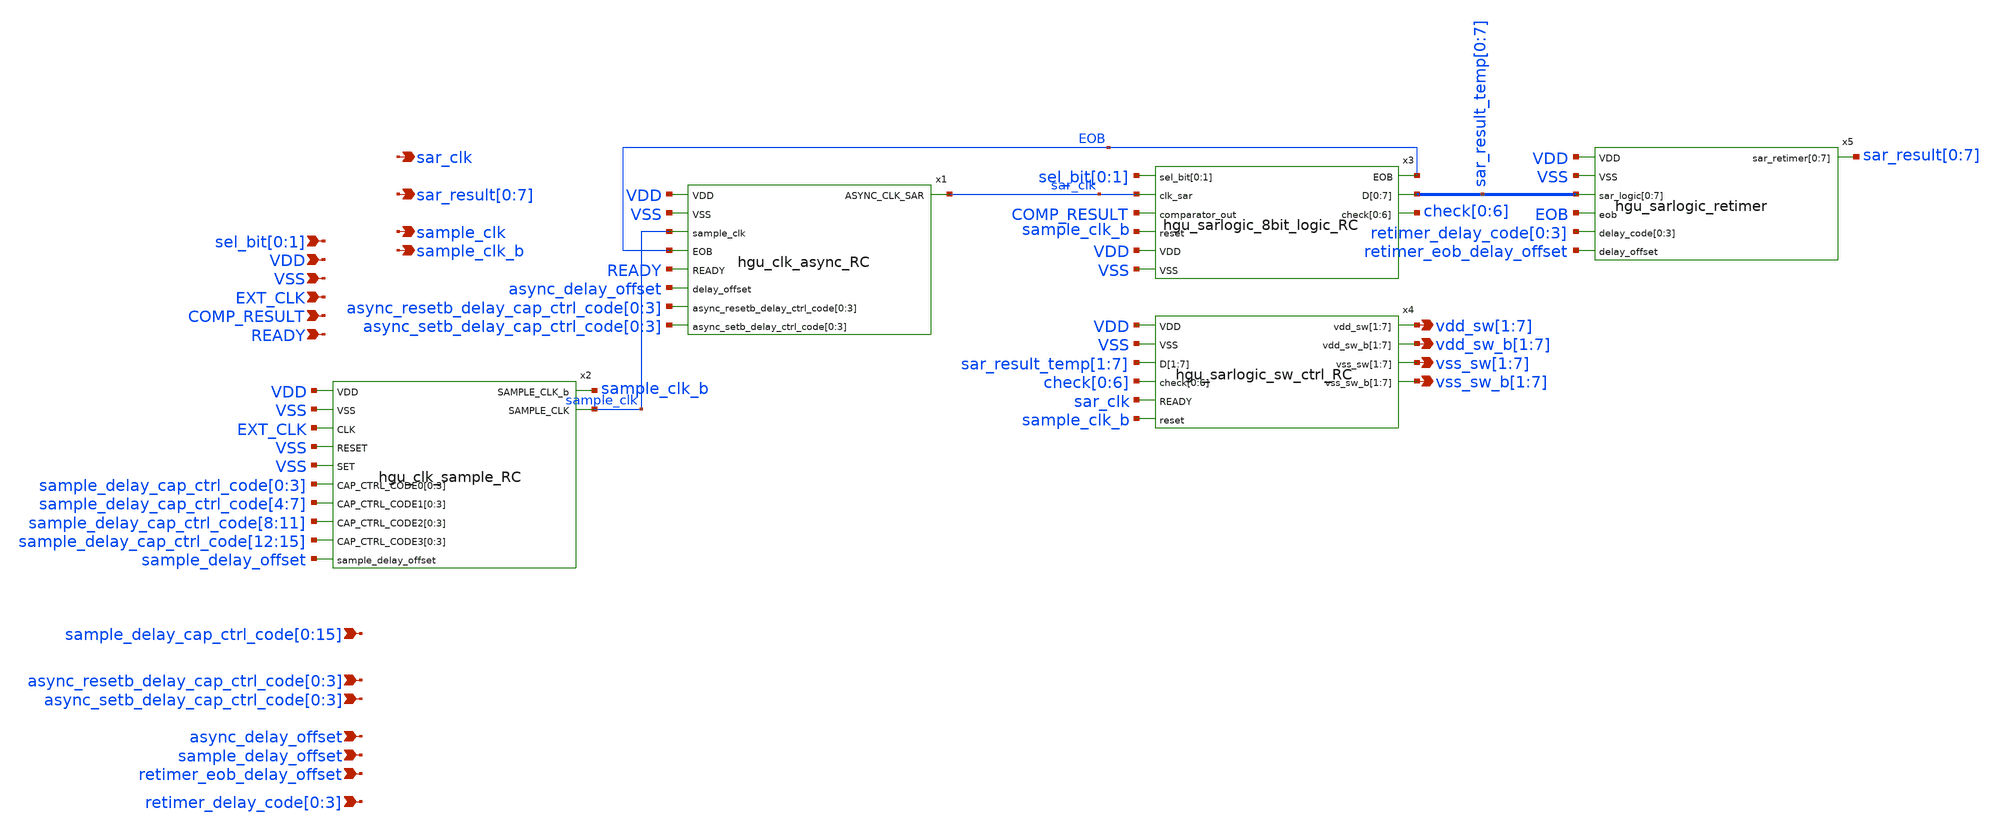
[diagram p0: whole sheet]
** sch_path: hgu/xschem/hgu_sarlogic_RC.sch
**.subckt hgu_sarlogic_RC VDD VSS COMP_RESULT READY EXT_CLK sar_clk
*+ sar_result[0],sar_result[1],sar_result[2],sar_result[3],sar_result[4],sar_result[5],sar_result[6],sar_result[7] sample_clk sel_bit[0],sel_bit[1]
*+ sample_delay_cap_ctrl_code[0],sample_delay_cap_ctrl_code[1],sample_delay_cap_ctrl_code[2],sample_delay_cap_ctrl_code[3],sample_delay_cap_ctrl_code[4],sample_delay_cap_ctrl_code[5],sample_delay_cap_ctrl_code[6],sample_delay_cap_ctrl_code[7],sample_delay_cap_ctrl_code[8],sample_delay_cap_ctrl_code[9],sample_delay_cap_ctrl_code[10],sample_delay_cap_ctrl_code[11],sample_delay_cap_ctrl_code[12],sample_delay_cap_ctrl_code[13],sample_delay_cap_ctrl_code[14],sample_delay_cap_ctrl_code[15] sample_clk_b vdd_sw[1],vdd_sw[2],vdd_sw[3],vdd_sw[4],vdd_sw[5],vdd_sw[6],vdd_sw[7]
*+ vdd_sw_b[1],vdd_sw_b[2],vdd_sw_b[3],vdd_sw_b[4],vdd_sw_b[5],vdd_sw_b[6],vdd_sw_b[7] vss_sw[1],vss_sw[2],vss_sw[3],vss_sw[4],vss_sw[5],vss_sw[6],vss_sw[7]
*+ vss_sw_b[1],vss_sw_b[2],vss_sw_b[3],vss_sw_b[4],vss_sw_b[5],vss_sw_b[6],vss_sw_b[7]
*+ async_resetb_delay_cap_ctrl_code[0],async_resetb_delay_cap_ctrl_code[1],async_resetb_delay_cap_ctrl_code[2],async_resetb_delay_cap_ctrl_code[3]
*+ async_setb_delay_cap_ctrl_code[0],async_setb_delay_cap_ctrl_code[1],async_setb_delay_cap_ctrl_code[2],async_setb_delay_cap_ctrl_code[3] async_delay_offset sample_delay_offset
*+ retimer_delay_code[0],retimer_delay_code[1],retimer_delay_code[2],retimer_delay_code[3] retimer_eob_delay_offset
*.ipin VDD
*.ipin VSS
*.ipin COMP_RESULT
*.ipin READY
*.ipin EXT_CLK
*.opin sar_clk
*.opin
*+ sar_result[0],sar_result[1],sar_result[2],sar_result[3],sar_result[4],sar_result[5],sar_result[6],sar_result[7]
*.opin sample_clk
*.ipin sel_bit[0],sel_bit[1]
*.ipin
*+ sample_delay_cap_ctrl_code[0],sample_delay_cap_ctrl_code[1],sample_delay_cap_ctrl_code[2],sample_delay_cap_ctrl_code[3],sample_delay_cap_ctrl_code[4],sample_delay_cap_ctrl_code[5],sample_delay_cap_ctrl_code[6],sample_delay_cap_ctrl_code[7],sample_delay_cap_ctrl_code[8],sample_delay_cap_ctrl_code[9],sample_delay_cap_ctrl_code[10],sample_delay_cap_ctrl_code[11],sample_delay_cap_ctrl_code[12],sample_delay_cap_ctrl_code[13],sample_delay_cap_ctrl_code[14],sample_delay_cap_ctrl_code[15]
*.opin sample_clk_b
*.opin vdd_sw[1],vdd_sw[2],vdd_sw[3],vdd_sw[4],vdd_sw[5],vdd_sw[6],vdd_sw[7]
*.opin vdd_sw_b[1],vdd_sw_b[2],vdd_sw_b[3],vdd_sw_b[4],vdd_sw_b[5],vdd_sw_b[6],vdd_sw_b[7]
*.opin vss_sw[1],vss_sw[2],vss_sw[3],vss_sw[4],vss_sw[5],vss_sw[6],vss_sw[7]
*.opin vss_sw_b[1],vss_sw_b[2],vss_sw_b[3],vss_sw_b[4],vss_sw_b[5],vss_sw_b[6],vss_sw_b[7]
*.ipin
*+ async_resetb_delay_cap_ctrl_code[0],async_resetb_delay_cap_ctrl_code[1],async_resetb_delay_cap_ctrl_code[2],async_resetb_delay_cap_ctrl_code[3]
*.ipin
*+ async_setb_delay_cap_ctrl_code[0],async_setb_delay_cap_ctrl_code[1],async_setb_delay_cap_ctrl_code[2],async_setb_delay_cap_ctrl_code[3]
*.ipin async_delay_offset
*.ipin sample_delay_offset
*.ipin retimer_delay_code[0],retimer_delay_code[1],retimer_delay_code[2],retimer_delay_code[3]
*.ipin retimer_eob_delay_offset
x1 sar_clk VDD VSS sample_clk EOB READY async_delay_offset async_resetb_delay_cap_ctrl_code[0]
+ async_resetb_delay_cap_ctrl_code[1] async_resetb_delay_cap_ctrl_code[2] async_resetb_delay_cap_ctrl_code[3]
+ async_setb_delay_cap_ctrl_code[0] async_setb_delay_cap_ctrl_code[1] async_setb_delay_cap_ctrl_code[2]
+ async_setb_delay_cap_ctrl_code[3] hgu_clk_async_RC
x2 sample_clk_b VDD VSS EXT_CLK VSS VSS sample_clk sample_delay_cap_ctrl_code[0]
+ sample_delay_cap_ctrl_code[1] sample_delay_cap_ctrl_code[2] sample_delay_cap_ctrl_code[3] sample_delay_cap_ctrl_code[4]
+ sample_delay_cap_ctrl_code[5] sample_delay_cap_ctrl_code[6] sample_delay_cap_ctrl_code[7] sample_delay_cap_ctrl_code[8]
+ sample_delay_cap_ctrl_code[9] sample_delay_cap_ctrl_code[10] sample_delay_cap_ctrl_code[11] sample_delay_cap_ctrl_code[12]
+ sample_delay_cap_ctrl_code[13] sample_delay_cap_ctrl_code[14] sample_delay_cap_ctrl_code[15] sample_delay_offset hgu_clk_sample_RC
x3 sel_bit[0] sel_bit[1] EOB sar_clk sar_result_temp[0] sar_result_temp[1] sar_result_temp[2]
+ sar_result_temp[3] sar_result_temp[4] sar_result_temp[5] sar_result_temp[6] sar_result_temp[7] COMP_RESULT check[0]
+ check[1] check[2] check[3] check[4] check[5] check[6] sample_clk_b VDD VSS hgu_sarlogic_8bit_logic_RC
x4 VDD VSS vdd_sw[1] vdd_sw[2] vdd_sw[3] vdd_sw[4] vdd_sw[5] vdd_sw[6] vdd_sw[7] vdd_sw_b[1]
+ vdd_sw_b[2] vdd_sw_b[3] vdd_sw_b[4] vdd_sw_b[5] vdd_sw_b[6] vdd_sw_b[7] sar_result_temp[1] sar_result_temp[2]
+ sar_result_temp[3] sar_result_temp[4] sar_result_temp[5] sar_result_temp[6] sar_result_temp[7] vss_sw[1] vss_sw[2]
+ vss_sw[3] vss_sw[4] vss_sw[5] vss_sw[6] vss_sw[7] check[0] check[1] check[2] check[3] check[4] check[5]
+ check[6] vss_sw_b[1] vss_sw_b[2] vss_sw_b[3] vss_sw_b[4] vss_sw_b[5] vss_sw_b[6] vss_sw_b[7] sar_clk
+ sample_clk_b hgu_sarlogic_sw_ctrl_RC
x5 VDD VSS sar_result_temp[0] sar_result_temp[1] sar_result_temp[2] sar_result_temp[3]
+ sar_result_temp[4] sar_result_temp[5] sar_result_temp[6] sar_result_temp[7] EOB retimer_delay_code[0]
+ retimer_delay_code[1] retimer_delay_code[2] retimer_delay_code[3] retimer_eob_delay_offset sar_result[0] sar_result[1]
+ sar_result[2] sar_result[3] sar_result[4] sar_result[5] sar_result[6] sar_result[7] hgu_sarlogic_retimer
**.ends
.end
